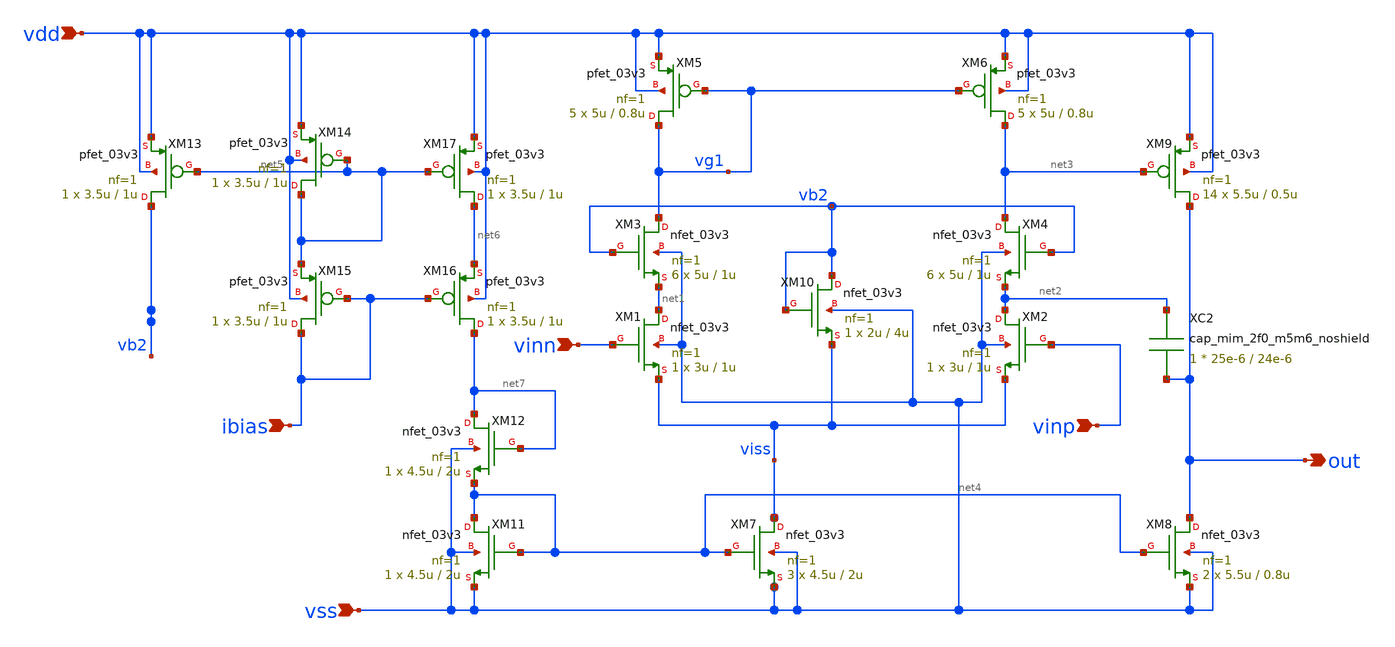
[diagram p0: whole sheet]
** sch_path: designs/libs/core_analog/opamp/opamp_n_input.sch
**.subckt opamp_n_input out vdd vss vinn ibias vinp
*.opin out
*.ipin vdd
*.ipin vss
*.ipin vinn
*.ipin ibias
*.ipin vinp
XM1 net1 vinn viss vss nfet_03v3 L=1u W=3u nf=1 ad='int((nf+1)/2) * W/nf * 0.18u' as='int((nf+2)/2) * W/nf * 0.18u'
+ pd='2*int((nf+1)/2) * (W/nf + 0.18u)' ps='2*int((nf+2)/2) * (W/nf + 0.18u)' nrd='0.18u / W' nrs='0.18u / W'
+ sa=0 sb=0 sd=0 m=1
XM2 net2 vinp viss vss nfet_03v3 L=1u W=3u nf=1 ad='int((nf+1)/2) * W/nf * 0.18u' as='int((nf+2)/2) * W/nf * 0.18u'
+ pd='2*int((nf+1)/2) * (W/nf + 0.18u)' ps='2*int((nf+2)/2) * (W/nf + 0.18u)' nrd='0.18u / W' nrs='0.18u / W'
+ sa=0 sb=0 sd=0 m=1
XM6 net3 vg1 vdd vdd pfet_03v3 L=0.8u W=5u nf=1 ad='int((nf+1)/2) * W/nf * 0.18u' as='int((nf+2)/2) * W/nf * 0.18u'
+ pd='2*int((nf+1)/2) * (W/nf + 0.18u)' ps='2*int((nf+2)/2) * (W/nf + 0.18u)' nrd='0.18u / W' nrs='0.18u / W'
+ sa=0 sb=0 sd=0 m=5
XM5 vg1 vg1 vdd vdd pfet_03v3 L=0.8u W=5u nf=1 ad='int((nf+1)/2) * W/nf * 0.18u' as='int((nf+2)/2) * W/nf * 0.18u'
+ pd='2*int((nf+1)/2) * (W/nf + 0.18u)' ps='2*int((nf+2)/2) * (W/nf + 0.18u)' nrd='0.18u / W' nrs='0.18u / W'
+ sa=0 sb=0 sd=0 m=5
XM4 net3 vb2 net2 vss nfet_03v3 L=1u W=5u nf=1 ad='int((nf+1)/2) * W/nf * 0.18u' as='int((nf+2)/2) * W/nf * 0.18u'
+ pd='2*int((nf+1)/2) * (W/nf + 0.18u)' ps='2*int((nf+2)/2) * (W/nf + 0.18u)' nrd='0.18u / W' nrs='0.18u / W'
+ sa=0 sb=0 sd=0 m=6
XM3 vg1 vb2 net1 vss nfet_03v3 L=1u W=5u nf=1 ad='int((nf+1)/2) * W/nf * 0.18u' as='int((nf+2)/2) * W/nf * 0.18u'
+ pd='2*int((nf+1)/2) * (W/nf + 0.18u)' ps='2*int((nf+2)/2) * (W/nf + 0.18u)' nrd='0.18u / W' nrs='0.18u / W'
+ sa=0 sb=0 sd=0 m=6
XM7 viss net4 vss vss nfet_03v3 L=2u W=4.5u nf=1 ad='int((nf+1)/2) * W/nf * 0.18u' as='int((nf+2)/2) * W/nf * 0.18u'
+ pd='2*int((nf+1)/2) * (W/nf + 0.18u)' ps='2*int((nf+2)/2) * (W/nf + 0.18u)' nrd='0.18u / W' nrs='0.18u / W'
+ sa=0 sb=0 sd=0 m=3
XM11 net4 net4 vss vss nfet_03v3 L=2u W=4.5u nf=1 ad='int((nf+1)/2) * W/nf * 0.18u' as='int((nf+2)/2) * W/nf * 0.18u'
+ pd='2*int((nf+1)/2) * (W/nf + 0.18u)' ps='2*int((nf+2)/2) * (W/nf + 0.18u)' nrd='0.18u / W' nrs='0.18u / W'
+ sa=0 sb=0 sd=0 m=1
XM10 vb2 vb2 viss vss nfet_03v3 L=4u W=2u nf=1 ad='int((nf+1)/2) * W/nf * 0.18u' as='int((nf+2)/2) * W/nf * 0.18u'
+ pd='2*int((nf+1)/2) * (W/nf + 0.18u)' ps='2*int((nf+2)/2) * (W/nf + 0.18u)' nrd='0.18u / W' nrs='0.18u / W'
+ sa=0 sb=0 sd=0 m=1
XM8 out net4 vss vss nfet_03v3 L=0.8u W=5.5u nf=1 ad='int((nf+1)/2) * W/nf * 0.18u' as='int((nf+2)/2) * W/nf * 0.18u'
+ pd='2*int((nf+1)/2) * (W/nf + 0.18u)' ps='2*int((nf+2)/2) * (W/nf + 0.18u)' nrd='0.18u / W' nrs='0.18u / W'
+ sa=0 sb=0 sd=0 m=2
XM9 out net3 vdd vdd pfet_03v3 L=0.5u W=5.5u nf=1 ad='int((nf+1)/2) * W/nf * 0.18u' as='int((nf+2)/2) * W/nf * 0.18u'
+ pd='2*int((nf+1)/2) * (W/nf + 0.18u)' ps='2*int((nf+2)/2) * (W/nf + 0.18u)' nrd='0.18u / W' nrs='0.18u / W'
+ sa=0 sb=0 sd=0 m=14
XM12 net7 net7 net4 vss nfet_03v3 L=2u W=4.5u nf=1 ad='int((nf+1)/2) * W/nf * 0.18u' as='int((nf+2)/2) * W/nf * 0.18u'
+ pd='2*int((nf+1)/2) * (W/nf + 0.18u)' ps='2*int((nf+2)/2) * (W/nf + 0.18u)' nrd='0.18u / W' nrs='0.18u / W'
+ sa=0 sb=0 sd=0 m=1
XM13 vb2 net5 vdd vdd pfet_03v3 L=1u W=3.5u nf=1 ad='int((nf+1)/2) * W/nf * 0.18u' as='int((nf+2)/2) * W/nf * 0.18u'
+ pd='2*int((nf+1)/2) * (W/nf + 0.18u)' ps='2*int((nf+2)/2) * (W/nf + 0.18u)' nrd='0.18u / W' nrs='0.18u / W'
+ sa=0 sb=0 sd=0 m=1
XM14 net5 net5 vdd vdd pfet_03v3 L=1u W=3.5u nf=1 ad='int((nf+1)/2) * W/nf * 0.18u' as='int((nf+2)/2) * W/nf * 0.18u'
+ pd='2*int((nf+1)/2) * (W/nf + 0.18u)' ps='2*int((nf+2)/2) * (W/nf + 0.18u)' nrd='0.18u / W' nrs='0.18u / W'
+ sa=0 sb=0 sd=0 m=1
XM15 ibias ibias net5 vdd pfet_03v3 L=1u W=3.5u nf=1 ad='int((nf+1)/2) * W/nf * 0.18u' as='int((nf+2)/2) * W/nf * 0.18u'
+ pd='2*int((nf+1)/2) * (W/nf + 0.18u)' ps='2*int((nf+2)/2) * (W/nf + 0.18u)' nrd='0.18u / W' nrs='0.18u / W'
+ sa=0 sb=0 sd=0 m=1
XM16 net7 ibias net6 vdd pfet_03v3 L=1u W=3.5u nf=1 ad='int((nf+1)/2) * W/nf * 0.18u' as='int((nf+2)/2) * W/nf * 0.18u'
+ pd='2*int((nf+1)/2) * (W/nf + 0.18u)' ps='2*int((nf+2)/2) * (W/nf + 0.18u)' nrd='0.18u / W' nrs='0.18u / W'
+ sa=0 sb=0 sd=0 m=1
XM17 net6 net5 vdd vdd pfet_03v3 L=1u W=3.5u nf=1 ad='int((nf+1)/2) * W/nf * 0.18u' as='int((nf+2)/2) * W/nf * 0.18u'
+ pd='2*int((nf+1)/2) * (W/nf + 0.18u)' ps='2*int((nf+2)/2) * (W/nf + 0.18u)' nrd='0.18u / W' nrs='0.18u / W'
+ sa=0 sb=0 sd=0 m=1
XC2 net2 out cap_mim_2f0_m5m6_noshield c_width=25e-6 c_length=24e-6 m=1
**.ends
.end
